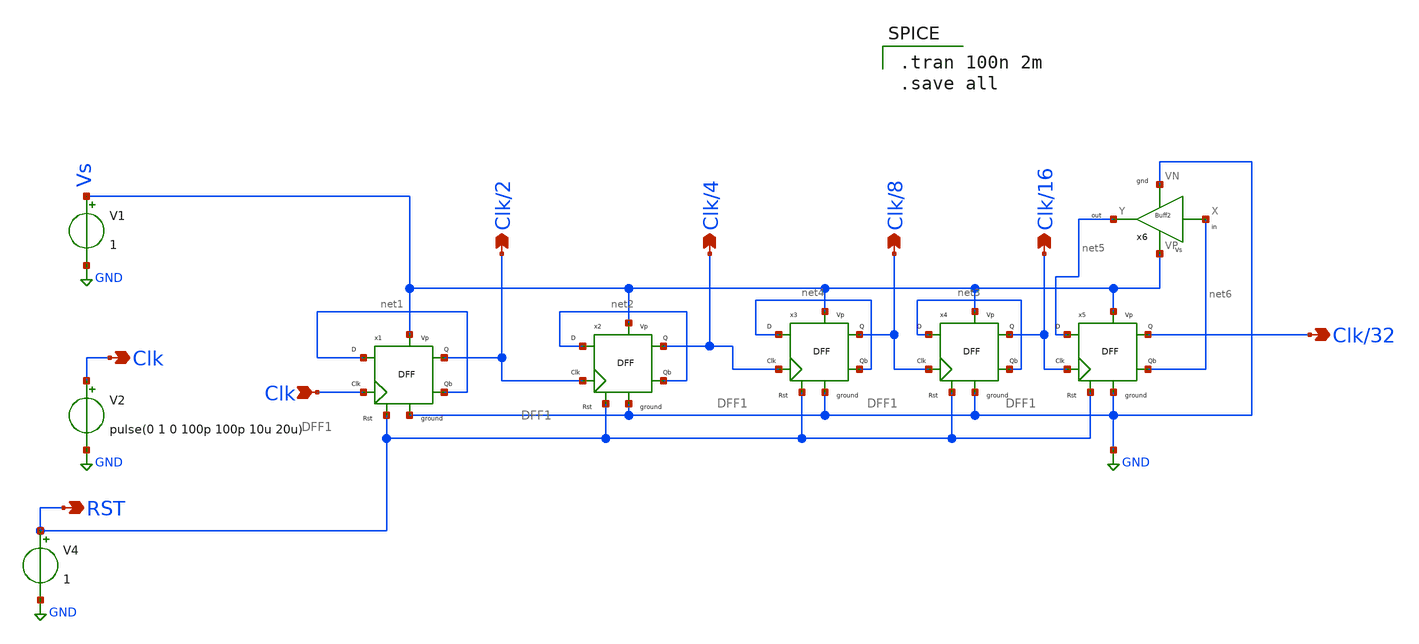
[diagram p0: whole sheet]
** sch_path: Blocks/Divide by 3 Circuit/div_by_2,4,8,16,32.sch
**.subckt div_by_2,4,8,16,32 Clk Clk/32 Clk RST Clk/2 Clk/4 Clk/8 Clk/16
*.opin Clk
*.opin Clk/32
*.ipin Clk
*.opin RST
*.opin Clk/2
*.opin Clk/4
*.opin Clk/8
*.opin Clk/16
x1 net1 Clk RST GND Vs Clk/2 net1 DFF1
V1 Vs GND 1
V2 Clk GND pulse(0 1 0 100p 100p 10u 20u)
V4 RST GND 1
x2 net2 Clk/2 RST GND Vs Clk/4 net2 DFF1
x3 net4 Clk/4 RST GND Vs Clk/8 net4 DFF1
x4 net3 Clk/8 RST GND Vs Clk/16 net3 DFF1
x5 net5 Clk/16 RST GND Vs Clk/32 net6 DFF1
x6 net6 net5 Vs GND Buff
**** begin user architecture code

** opencircuitdesign pdks install
.lib $::SKYWATER_MODELS/sky130.lib.spice tt



.tran 100n 2m
.save all

**** end user architecture code
**.ends

* expanding   symbol:  Pico_project/FlipFlops/DFF1.sym # of pins=7
** sym_path: component/FlipFlops/DFF1.sym
** sch_path: component/FlipFlops/DFF1.sch
.subckt DFF1 D Clk RST VN VP Q Qb
*.opin Q
*.iopin VN
*.iopin VP
*.ipin Clk
*.ipin D
*.ipin RST
*.opin Qb
x7 net2 net4 net3 VP VN NAND
x8 net3 Clk RST VP VN net2 NAND3
x6 Q net1 RST VP VN Qb NAND3
x4 net2 Clk net4 VP VN net1 NAND3
x5 net1 D RST VP VN net4 NAND3
x1 Qb net2 Q VP VN NAND
.ends


* expanding   symbol:  Pico_project/Buffer/Buff.sym # of pins=4
** sym_path: Blocks/Buffer/Buff.sym
** sch_path: Blocks/Buffer/Buff.sch
.subckt Buff X Y VP VN
*.ipin X
*.opin Y
*.iopin VN
*.iopin VP
x1 X net1 VP VN INV
x2 net1 Y VP VN INV
.ends


* expanding   symbol:  component/NAND2/NAND.sym # of pins=5
** sym_path: component/NAND2/NAND.sym
** sch_path: component/NAND2/NAND.sch
.subckt NAND B A Y VP VN
*.iopin VP
*.ipin A
*.ipin B
*.opin Y
*.iopin VN
XM1 Y A VP VP sky130_fd_pr__pfet_01v8 L=0.15 W=1.26 nf=1 ad='int((nf+1)/2) * W/nf * 0.29' as='int((nf+2)/2) * W/nf * 0.29'
+ pd='2*int((nf+1)/2) * (W/nf + 0.29)' ps='2*int((nf+2)/2) * (W/nf + 0.29)' nrd='0.29 / W' nrs='0.29 / W'
+ sa=0 sb=0 sd=0 mult=1 m=1
XM2 Y B VP VP sky130_fd_pr__pfet_01v8 L=0.15 W=1.26 nf=1 ad='int((nf+1)/2) * W/nf * 0.29' as='int((nf+2)/2) * W/nf * 0.29'
+ pd='2*int((nf+1)/2) * (W/nf + 0.29)' ps='2*int((nf+2)/2) * (W/nf + 0.29)' nrd='0.29 / W' nrs='0.29 / W'
+ sa=0 sb=0 sd=0 mult=1 m=1
XM3 Y A net1 net1 sky130_fd_pr__nfet_01v8 L=0.15 W=0.84 nf=1 ad='int((nf+1)/2) * W/nf * 0.29' as='int((nf+2)/2) * W/nf * 0.29'
+ pd='2*int((nf+1)/2) * (W/nf + 0.29)' ps='2*int((nf+2)/2) * (W/nf + 0.29)' nrd='0.29 / W' nrs='0.29 / W'
+ sa=0 sb=0 sd=0 mult=1 m=1
XM4 net1 B VN VN sky130_fd_pr__nfet_01v8 L=0.15 W=0.84 nf=1 ad='int((nf+1)/2) * W/nf * 0.29' as='int((nf+2)/2) * W/nf * 0.29'
+ pd='2*int((nf+1)/2) * (W/nf + 0.29)' ps='2*int((nf+2)/2) * (W/nf + 0.29)' nrd='0.29 / W' nrs='0.29 / W'
+ sa=0 sb=0 sd=0 mult=1 m=1
.ends


* expanding   symbol:  component/NAND3/NAND3.sym # of pins=6
** sym_path: component/NAND3/NAND3.sym
** sch_path: component/NAND3/NAND3.sch
.subckt NAND3 A B C VP VN Y
*.iopin VP
*.iopin VN
*.ipin A
*.ipin B
*.ipin C
*.opin Y
XM1 Y A net1 VN sky130_fd_pr__nfet_01v8 L=0.15 W=1.26 nf=1 ad='int((nf+1)/2) * W/nf * 0.29' as='int((nf+2)/2) * W/nf * 0.29'
+ pd='2*int((nf+1)/2) * (W/nf + 0.29)' ps='2*int((nf+2)/2) * (W/nf + 0.29)' nrd='0.29 / W' nrs='0.29 / W'
+ sa=0 sb=0 sd=0 mult=1 m=1
XM2 net1 B net2 VN sky130_fd_pr__nfet_01v8 L=0.15 W=1.26 nf=1 ad='int((nf+1)/2) * W/nf * 0.29' as='int((nf+2)/2) * W/nf * 0.29'
+ pd='2*int((nf+1)/2) * (W/nf + 0.29)' ps='2*int((nf+2)/2) * (W/nf + 0.29)' nrd='0.29 / W' nrs='0.29 / W'
+ sa=0 sb=0 sd=0 mult=1 m=1
XM3 net2 C VN VN sky130_fd_pr__nfet_01v8 L=0.15 W=1.26 nf=1 ad='int((nf+1)/2) * W/nf * 0.29' as='int((nf+2)/2) * W/nf * 0.29'
+ pd='2*int((nf+1)/2) * (W/nf + 0.29)' ps='2*int((nf+2)/2) * (W/nf + 0.29)' nrd='0.29 / W' nrs='0.29 / W'
+ sa=0 sb=0 sd=0 mult=1 m=1
XM4 Y A VP VP sky130_fd_pr__pfet_01v8 L=0.15 W=1.26 nf=1 ad='int((nf+1)/2) * W/nf * 0.29' as='int((nf+2)/2) * W/nf * 0.29'
+ pd='2*int((nf+1)/2) * (W/nf + 0.29)' ps='2*int((nf+2)/2) * (W/nf + 0.29)' nrd='0.29 / W' nrs='0.29 / W'
+ sa=0 sb=0 sd=0 mult=1 m=1
XM5 Y B VP VP sky130_fd_pr__pfet_01v8 L=0.15 W=1.26 nf=1 ad='int((nf+1)/2) * W/nf * 0.29' as='int((nf+2)/2) * W/nf * 0.29'
+ pd='2*int((nf+1)/2) * (W/nf + 0.29)' ps='2*int((nf+2)/2) * (W/nf + 0.29)' nrd='0.29 / W' nrs='0.29 / W'
+ sa=0 sb=0 sd=0 mult=1 m=1
XM6 Y C VP VP sky130_fd_pr__pfet_01v8 L=0.15 W=1.26 nf=1 ad='int((nf+1)/2) * W/nf * 0.29' as='int((nf+2)/2) * W/nf * 0.29'
+ pd='2*int((nf+1)/2) * (W/nf + 0.29)' ps='2*int((nf+2)/2) * (W/nf + 0.29)' nrd='0.29 / W' nrs='0.29 / W'
+ sa=0 sb=0 sd=0 mult=1 m=1
.ends


* expanding   symbol:  Pico_project/INV/INV.sym # of pins=4
** sym_path: component/INV/INV.sym
** sch_path: component/INV/INV.sch
.subckt INV X Y VP VN
*.ipin X
*.opin Y
*.iopin VN
*.iopin VP
XM1 Y X VN VN sky130_fd_pr__nfet_01v8 L=0.15 W=0.42 nf=1 ad='int((nf+1)/2) * W/nf * 0.29' as='int((nf+2)/2) * W/nf * 0.29'
+ pd='2*int((nf+1)/2) * (W/nf + 0.29)' ps='2*int((nf+2)/2) * (W/nf + 0.29)' nrd='0.29 / W' nrs='0.29 / W'
+ sa=0 sb=0 sd=0 mult=1 m=1
XM2 Y X VP VP sky130_fd_pr__pfet_01v8 L=0.15 W=1.26 nf=1 ad='int((nf+1)/2) * W/nf * 0.29' as='int((nf+2)/2) * W/nf * 0.29'
+ pd='2*int((nf+1)/2) * (W/nf + 0.29)' ps='2*int((nf+2)/2) * (W/nf + 0.29)' nrd='0.29 / W' nrs='0.29 / W'
+ sa=0 sb=0 sd=0 mult=1 m=1
.ends

.GLOBAL GND
.end
